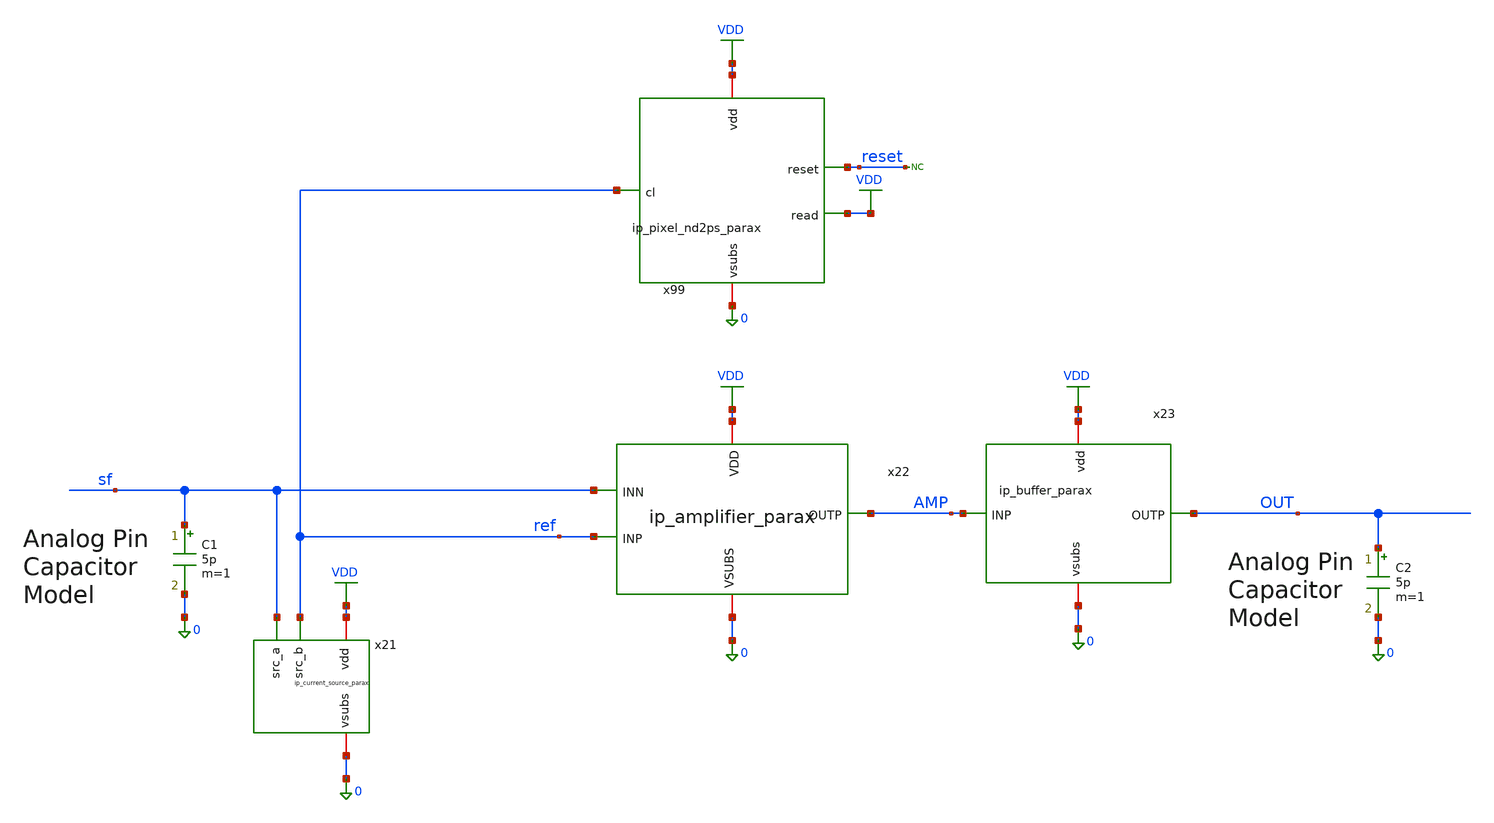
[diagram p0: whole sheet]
** sch_path: xschem/tb_total_tran.sch
**.subckt tb_total_tran
x21 VDD sf 0 ref ip_current_source_parax
x22 VDD AMP ref sf 0 ip_amplifier_parax
x99 VDD reset VDD 0 ref ip_pixel_nd2ps_parax
C1 sf 0 5p m=1
x23 VDD OUT AMP 0 ip_buffer_parax
C2 OUT 0 5p m=1
* noconn reset
**** begin user architecture code

.include $::180MCU_MODELS/design.ngspice
.lib $::180MCU_MODELS/sm141064.ngspice typical
.lib $::180MCU_MODELS/sm141064.ngspice res_typical
.lib $::180MCU_MODELS/sm141064.ngspice moscap_typical
.lib $::180MCU_MODELS/sm141064.ngspice diode_typical




.option klu
.option reltol=0.05
.option abstol=100u
.save none

.save V(nRA0) V(nRA1) V(nRA2) V(nRA3) V(nRA4)
.save V(nCA0) V(nCA1) V(nCA2) V(nCA3) V(nCA4)

.save V(ncy0) V(ncy1) V(ncy2) V(ncy3) V(ncy4) V(ncy5) V(ncy6) V(ncy7) V(ncy8)
.save V(ncy9) V(ncy10) V(ncy11) V(ncy12) V(ncy13) V(ncy14) V(ncy15) V(ncy16)
.save V(ncy17) V(ncy18) V(ncy19) V(ncy20)

.save V(nry0) V(nry1) V(nry2) V(nry3) V(nry4) V(nry5) V(nry6) V(nry7) V(nry8)
.save V(nry9) V(nry10) V(nry11) V(nry12) V(nry13) V(nry14) V(nry15) V(nry16)

.save V(reset) V(clk)
.save V(out) V(sf) V(ref) V(amp)
.control
	reset
	tran 100n 5.2m 0 100n
	write tb_total_tran.raw
	quit
.endc






VVDD VDD 0 3.3
VCLK CLK 0 PULSE (0 3.3 0 1n 1n 2u 4u)

astim [RESETA        dRA4 dRA3 dRA2 dRA1 dRA0        dCA4 dCA3 dCA2 dCA1 dCA0] stim
.model stim d_source input_file="../st_total.txt"

acosim[CLK        dCA4 dCA3 dCA2 dCA1 dCA0        dRA4 dRA3 dRA2 dRA1 dRA0        RESETA]
+        [dreset        dCY20 dCY19 dCY18 dCY17 dCY16 dCY15        dCY14 dCY13 dCY12 dCY11 dCY10 dCY9         dCY8
+  dCY7  dCY6  dCY5  dCY4  dCY3         dCY2  dCY1  dCY0         dRY16 dRY15 dRY14 dRY13 dRY12 dRY11
+         dRY10 dRY9  dRY8  dRY7  dRY6  dRY5        dRY4  dRY3  dRY2  dRY1  dRY0        ] null dut
.model dut d_cosim simulation="../../verilog/rtl/aux_total_digital/aux_total_digital.so"

.include pixels.spice


**** end user architecture code
**.ends

* expanding   symbol:  ip_current_source_parax.sym # of pins=4
** sym_path: xschem/ip_current_source.sym
.include [file normalize ./parax/ip_current_source.sim.spice]

* expanding   symbol:  ip_amplifier_parax.sym # of pins=5
** sym_path: xschem/ip_amplifier.sym
.include [file normalize ./parax/ip_amplifier.sim.spice]

* expanding   symbol:  ip_pixel_nd2ps_parax.sym # of pins=5
** sym_path: xschem/ip_pixel_nd2ps.sym
.include [file normalize ./parax/ip_pixel_nd2ps.sim.spice]

* expanding   symbol:  ip_buffer_parax.sym # of pins=4
** sym_path: xschem/ip_buffer.sym
.include [file normalize ./parax/ip_buffer.sim.spice]
.GLOBAL VDD
.end
